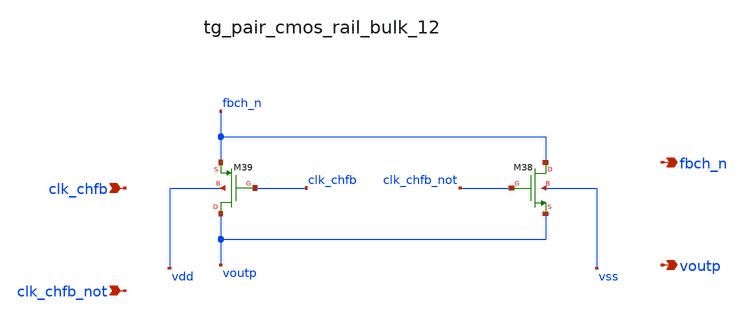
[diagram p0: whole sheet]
** sch_path: analog-db/raw/ia_002_fan_chopper_simple/hier/blocks/tg_pair_cmos_rail_bulk_12.sch
**.subckt tg_pair_cmos_rail_bulk_12 clk_chfb clk_chfb_not fbch_n voutp
*.ipin clk_chfb
*.ipin clk_chfb_not
*.opin fbch_n
*.opin voutp
XM38 fbch_n clk_chfb_not voutp vss sg13_lv_nmos w=x_dut_xm38_w l=x_dut_xm38_l ng=1 m=x_dut_xm38_m
XM39 voutp clk_chfb fbch_n vdd sg13_lv_pmos w=x_dut_xm39_w l=x_dut_xm39_l ng=1 m=x_dut_xm39_m
**.ends
.end
